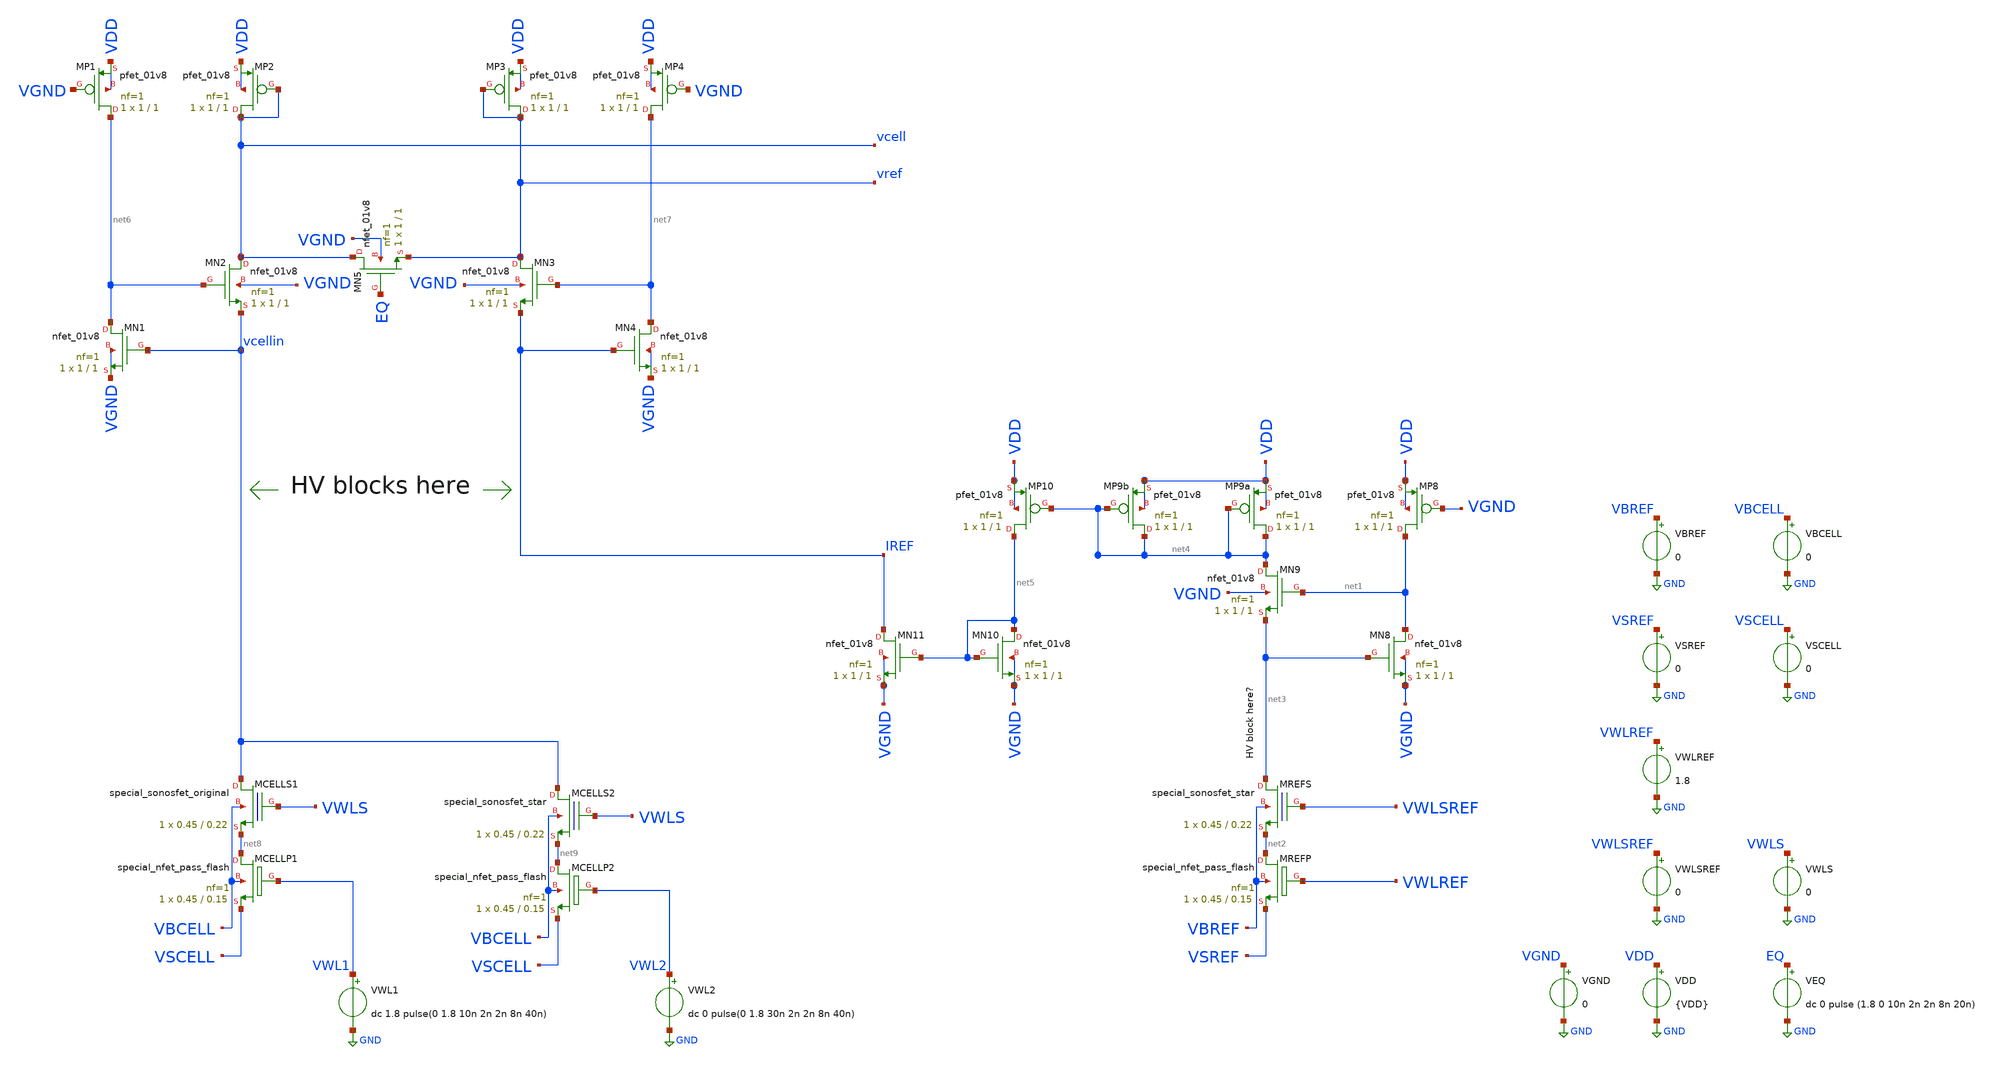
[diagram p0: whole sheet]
** sch_path: read/bg_read_complete.sch
**.subckt bg_read_complete
XMN8 net1 net3 VGND VGND sky130_fd_pr__nfet_01v8 L=1 W=1 nf=1 ad='int((nf+1)/2) * W/nf * 0.29' as='int((nf+2)/2) * W/nf * 0.29'
+ pd='2*int((nf+1)/2) * (W/nf + 0.29)' ps='2*int((nf+2)/2) * (W/nf + 0.29)' nrd='0.29 / W' nrs='0.29 / W'
+ sa=0 sb=0 sd=0 mult=1 m=1
XMP8 net1 VGND VDD VDD sky130_fd_pr__pfet_01v8 L=1 W=1 nf=1 ad='int((nf+1)/2) * W/nf * 0.29' as='int((nf+2)/2) * W/nf * 0.29'
+ pd='2*int((nf+1)/2) * (W/nf + 0.29)' ps='2*int((nf+2)/2) * (W/nf + 0.29)' nrd='0.29 / W' nrs='0.29 / W'
+ sa=0 sb=0 sd=0 mult=1 m=1
XMN9 net4 net1 net3 VGND sky130_fd_pr__nfet_01v8 L=1 W=1 nf=1 ad='int((nf+1)/2) * W/nf * 0.29' as='int((nf+2)/2) * W/nf * 0.29'
+ pd='2*int((nf+1)/2) * (W/nf + 0.29)' ps='2*int((nf+2)/2) * (W/nf + 0.29)' nrd='0.29 / W' nrs='0.29 / W'
+ sa=0 sb=0 sd=0 mult=1 m=1
XMREFS net3 VWLSREF net2 VBREF sky130_fd_bs_flash__special_sonosfet_star L=0.22 W=0.45 nf=1 ad='1 * W * 0.29'
+ as='1 * W * 0.29' pd='2 * (W + 0.29)' ps='2 * (W + 0.29)' nrd='0.29 / W' nrs='0.29 / W' sa=0 sb=0 sd=0
+ mult=1 m=1
XMREFP net2 VWLREF VSREF VBREF sky130_fd_pr__special_nfet_pass_flash L=0.15 W=0.45 nf=1 ad='1 * W * 0.29'
+ as='1 * W * 0.29' pd='2 * (W + 0.29)' ps='2 * (W + 0.29)' nrd='0.29 / W' nrs='0.29 / W' sa=0 sb=0 sd=0
+ mult=1 m=1
XMP9a net4 net4 VDD VDD sky130_fd_pr__pfet_01v8 L=1 W=1 nf=1 ad='int((nf+1)/2) * W/nf * 0.29' as='int((nf+2)/2) * W/nf * 0.29'
+ pd='2*int((nf+1)/2) * (W/nf + 0.29)' ps='2*int((nf+2)/2) * (W/nf + 0.29)' nrd='0.29 / W' nrs='0.29 / W'
+ sa=0 sb=0 sd=0 mult=1 m=1
XMP10 net5 net4 VDD VDD sky130_fd_pr__pfet_01v8 L=1 W=1 nf=1 ad='int((nf+1)/2) * W/nf * 0.29' as='int((nf+2)/2) * W/nf * 0.29'
+ pd='2*int((nf+1)/2) * (W/nf + 0.29)' ps='2*int((nf+2)/2) * (W/nf + 0.29)' nrd='0.29 / W' nrs='0.29 / W'
+ sa=0 sb=0 sd=0 mult=1 m=1
XMN10 net5 net5 VGND VGND sky130_fd_pr__nfet_01v8 L=1 W=1 nf=1 ad='int((nf+1)/2) * W/nf * 0.29' as='int((nf+2)/2) * W/nf * 0.29'
+ pd='2*int((nf+1)/2) * (W/nf + 0.29)' ps='2*int((nf+2)/2) * (W/nf + 0.29)' nrd='0.29 / W' nrs='0.29 / W'
+ sa=0 sb=0 sd=0 mult=1 m=1
XMN11 IREF net5 VGND VGND sky130_fd_pr__nfet_01v8 L=1 W=1 nf=1 ad='int((nf+1)/2) * W/nf * 0.29' as='int((nf+2)/2) * W/nf * 0.29'
+ pd='2*int((nf+1)/2) * (W/nf + 0.29)' ps='2*int((nf+2)/2) * (W/nf + 0.29)' nrd='0.29 / W' nrs='0.29 / W'
+ sa=0 sb=0 sd=0 mult=1 m=1
XMP9b net4 net4 VDD VDD sky130_fd_pr__pfet_01v8 L=1 W=1 nf=1 ad='int((nf+1)/2) * W/nf * 0.29' as='int((nf+2)/2) * W/nf * 0.29'
+ pd='2*int((nf+1)/2) * (W/nf + 0.29)' ps='2*int((nf+2)/2) * (W/nf + 0.29)' nrd='0.29 / W' nrs='0.29 / W'
+ sa=0 sb=0 sd=0 mult=1 m=1
VDD VDD GND {VDD}
VGND VGND GND 0
VWLSREF VWLSREF GND 0
VWLREF VWLREF GND 1.8
VSREF VSREF GND 0
VBREF VBREF GND 0
XMN1 net6 vcellin VGND VGND sky130_fd_pr__nfet_01v8 L=1 W=1 nf=1 ad='int((nf+1)/2) * W/nf * 0.29' as='int((nf+2)/2) * W/nf * 0.29'
+ pd='2*int((nf+1)/2) * (W/nf + 0.29)' ps='2*int((nf+2)/2) * (W/nf + 0.29)' nrd='0.29 / W' nrs='0.29 / W'
+ sa=0 sb=0 sd=0 mult=1 m=1
XMP1 net6 VGND VDD VDD sky130_fd_pr__pfet_01v8 L=1 W=1 nf=1 ad='int((nf+1)/2) * W/nf * 0.29' as='int((nf+2)/2) * W/nf * 0.29'
+ pd='2*int((nf+1)/2) * (W/nf + 0.29)' ps='2*int((nf+2)/2) * (W/nf + 0.29)' nrd='0.29 / W' nrs='0.29 / W'
+ sa=0 sb=0 sd=0 mult=1 m=1
XMN2 vcell net6 vcellin VGND sky130_fd_pr__nfet_01v8 L=1 W=1 nf=1 ad='int((nf+1)/2) * W/nf * 0.29' as='int((nf+2)/2) * W/nf * 0.29'
+ pd='2*int((nf+1)/2) * (W/nf + 0.29)' ps='2*int((nf+2)/2) * (W/nf + 0.29)' nrd='0.29 / W' nrs='0.29 / W'
+ sa=0 sb=0 sd=0 mult=1 m=1
XMP2 vcell vcell VDD VDD sky130_fd_pr__pfet_01v8 L=1 W=1 nf=1 ad='int((nf+1)/2) * W/nf * 0.29' as='int((nf+2)/2) * W/nf * 0.29'
+ pd='2*int((nf+1)/2) * (W/nf + 0.29)' ps='2*int((nf+2)/2) * (W/nf + 0.29)' nrd='0.29 / W' nrs='0.29 / W'
+ sa=0 sb=0 sd=0 mult=1 m=1
XMN4 net7 IREF VGND VGND sky130_fd_pr__nfet_01v8 L=1 W=1 nf=1 ad='int((nf+1)/2) * W/nf * 0.29' as='int((nf+2)/2) * W/nf * 0.29'
+ pd='2*int((nf+1)/2) * (W/nf + 0.29)' ps='2*int((nf+2)/2) * (W/nf + 0.29)' nrd='0.29 / W' nrs='0.29 / W'
+ sa=0 sb=0 sd=0 mult=1 m=1
XMP4 net7 VGND VDD VDD sky130_fd_pr__pfet_01v8 L=1 W=1 nf=1 ad='int((nf+1)/2) * W/nf * 0.29' as='int((nf+2)/2) * W/nf * 0.29'
+ pd='2*int((nf+1)/2) * (W/nf + 0.29)' ps='2*int((nf+2)/2) * (W/nf + 0.29)' nrd='0.29 / W' nrs='0.29 / W'
+ sa=0 sb=0 sd=0 mult=1 m=1
XMN3 vref net7 IREF VGND sky130_fd_pr__nfet_01v8 L=1 W=1 nf=1 ad='int((nf+1)/2) * W/nf * 0.29' as='int((nf+2)/2) * W/nf * 0.29'
+ pd='2*int((nf+1)/2) * (W/nf + 0.29)' ps='2*int((nf+2)/2) * (W/nf + 0.29)' nrd='0.29 / W' nrs='0.29 / W'
+ sa=0 sb=0 sd=0 mult=1 m=1
XMP3 vref vref VDD VDD sky130_fd_pr__pfet_01v8 L=1 W=1 nf=1 ad='int((nf+1)/2) * W/nf * 0.29' as='int((nf+2)/2) * W/nf * 0.29'
+ pd='2*int((nf+1)/2) * (W/nf + 0.29)' ps='2*int((nf+2)/2) * (W/nf + 0.29)' nrd='0.29 / W' nrs='0.29 / W'
+ sa=0 sb=0 sd=0 mult=1 m=1
XMN5 vcell EQ vref VGND sky130_fd_pr__nfet_01v8 L=1 W=1 nf=1 ad='int((nf+1)/2) * W/nf * 0.29' as='int((nf+2)/2) * W/nf * 0.29'
+ pd='2*int((nf+1)/2) * (W/nf + 0.29)' ps='2*int((nf+2)/2) * (W/nf + 0.29)' nrd='0.29 / W' nrs='0.29 / W'
+ sa=0 sb=0 sd=0 mult=1 m=1
XMCELLS1 vcellin VWLS net8 VBCELL sky130_fd_bs_flash__special_sonosfet_original L=0.22 W=0.45 nf=1 ad='1 * W * 0.29'
+ as='1 * W * 0.29' pd='2 * (W + 0.29)' ps='2 * (W + 0.29)' nrd='0.29 / W' nrs='0.29 / W' sa=0 sb=0 sd=0
+ mult=1 m=1
XMCELLP1 net8 VWL1 VSCELL VBCELL sky130_fd_pr__special_nfet_pass_flash L=0.15 W=0.45 nf=1 ad='1 * W * 0.29'
+ as='1 * W * 0.29' pd='2 * (W + 0.29)' ps='2 * (W + 0.29)' nrd='0.29 / W' nrs='0.29 / W' sa=0 sb=0 sd=0
+ mult=1 m=1
VSCELL VSCELL GND 0
VBCELL VBCELL GND 0
VWLS VWLS GND 0
VWL1 VWL1 GND dc 1.8 pulse(0 1.8 10n 2n 2n 8n 40n)
VEQ EQ GND dc 0 pulse (1.8 0 10n 2n 2n 8n 20n)
XMCELLS2 vcellin VWLS net9 VBCELL sky130_fd_bs_flash__special_sonosfet_star L=0.22 W=0.45 nf=1 ad='1 * W * 0.29'
+ as='1 * W * 0.29' pd='2 * (W + 0.29)' ps='2 * (W + 0.29)' nrd='0.29 / W' nrs='0.29 / W' sa=0 sb=0 sd=0
+ mult=1 m=1
XMCELLP2 net9 VWL2 VSCELL VBCELL sky130_fd_pr__special_nfet_pass_flash L=0.15 W=0.45 nf=1 ad='1 * W * 0.29'
+ as='1 * W * 0.29' pd='2 * (W + 0.29)' ps='2 * (W + 0.29)' nrd='0.29 / W' nrs='0.29 / W' sa=0 sb=0 sd=0
+ mult=1 m=1
VWL2 VWL2 GND dc 0 pulse(0 1.8 30n 2n 2n 8n 40n)
**** begin user architecture code

** opencircuitdesign pdks install
.lib $::SKYWATER_MODELS/sky130.lib.spice tt
.include $::SKYWATER_MODELS/sonos_e/begin_of_life.spice
.include $::SKYWATER_MODELS/sonos_e/begin_of_life.pm3.spice
.include $::SKYWATER_MODELS/sonos_p/begin_of_life.spice
.include $::SKYWATER_MODELS/sonos_p/begin_of_life.pm3.spice



.param VDD=1.8
.option savecurrents
.control
  unset appendwrite
  save all
  op
  remzerovec
  write bg_read_complete.raw
  set appendwrite

  tran 0.2n 200n
  remzerovec
  write bg_read_complete.raw

  dc vwls 0 3 0.05
  remzerovec
  write bg_read_complete.raw
.endc


**** end user architecture code
**.ends
.GLOBAL GND
.end
